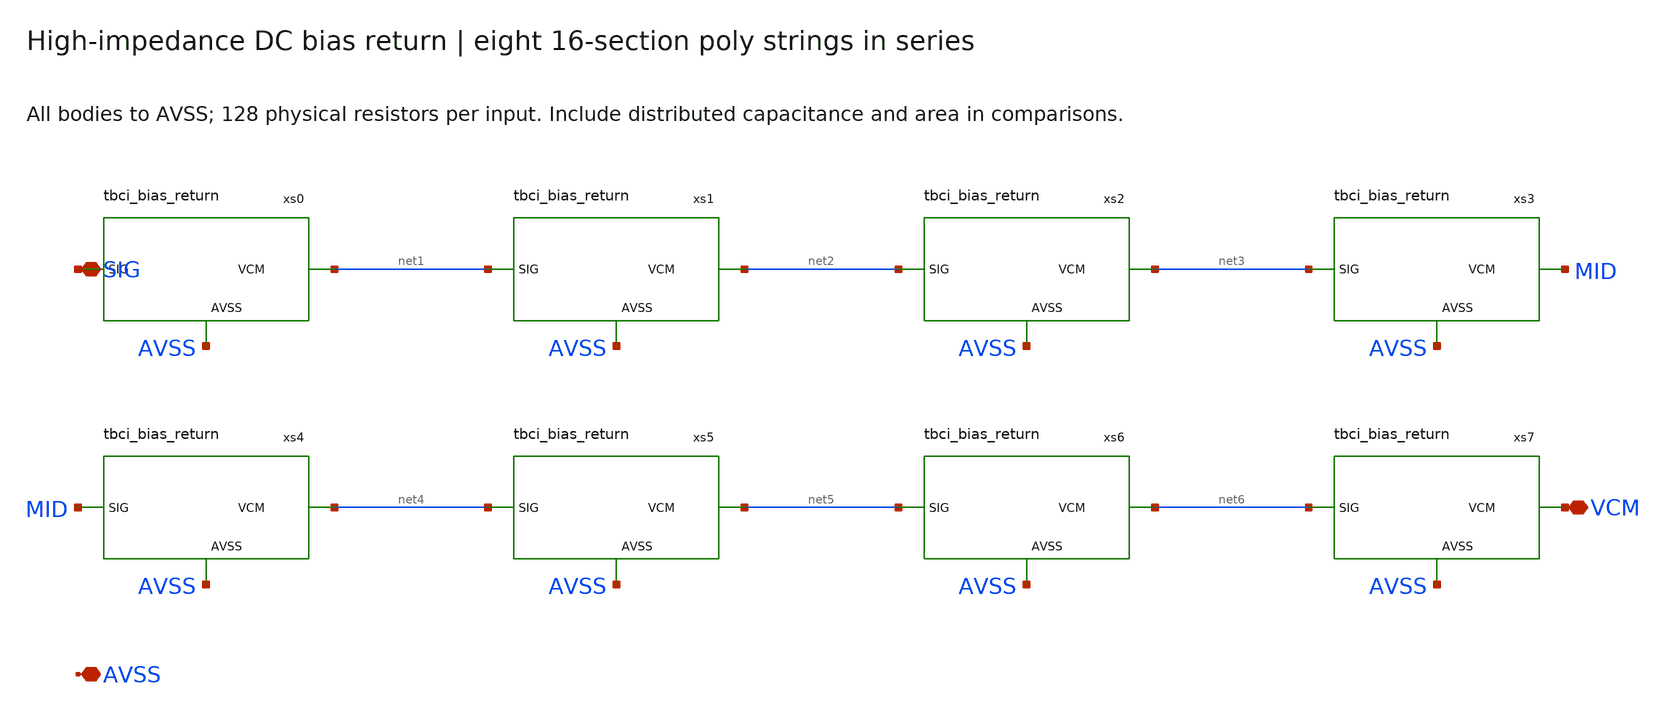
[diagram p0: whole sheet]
** sch_path: afe/xschem/tbci_bias_chain.sch
**.subckt tbci_bias_chain SIG VCM AVSS
*.iopin SIG
*.iopin VCM
*.iopin AVSS
xs0 SIG net1 AVSS tbci_bias_return
xs1 net1 net2 AVSS tbci_bias_return
xs2 net2 net3 AVSS tbci_bias_return
xs3 net3 MID AVSS tbci_bias_return
xs4 MID net4 AVSS tbci_bias_return
xs5 net4 net5 AVSS tbci_bias_return
xs6 net5 net6 AVSS tbci_bias_return
xs7 net6 VCM AVSS tbci_bias_return
**.ends

* expanding   symbol:  tbci_bias_return.sym # of pins=3
** sym_path: afe/xschem/tbci_bias_return.sym
** sch_path: afe/xschem/tbci_bias_return.sch
.subckt tbci_bias_return SIG VCM AVSS
*.iopin SIG
*.iopin VCM
*.iopin AVSS
XR0 net1 SIG AVSS sky130_fd_pr__res_xhigh_po_0p35 L=860 mult=1 m=1
XR1 net2 net1 AVSS sky130_fd_pr__res_xhigh_po_0p35 L=860 mult=1 m=1
XR2 net3 net2 AVSS sky130_fd_pr__res_xhigh_po_0p35 L=860 mult=1 m=1
XR3 net4 net3 AVSS sky130_fd_pr__res_xhigh_po_0p35 L=860 mult=1 m=1
XR4 net4 net5 AVSS sky130_fd_pr__res_xhigh_po_0p35 L=860 mult=1 m=1
XR5 net5 net6 AVSS sky130_fd_pr__res_xhigh_po_0p35 L=860 mult=1 m=1
XR6 net6 net7 AVSS sky130_fd_pr__res_xhigh_po_0p35 L=860 mult=1 m=1
XR7 net7 net8 AVSS sky130_fd_pr__res_xhigh_po_0p35 L=860 mult=1 m=1
XR8 net9 net8 AVSS sky130_fd_pr__res_xhigh_po_0p35 L=860 mult=1 m=1
XR9 net10 net9 AVSS sky130_fd_pr__res_xhigh_po_0p35 L=860 mult=1 m=1
XR10 net11 net10 AVSS sky130_fd_pr__res_xhigh_po_0p35 L=860 mult=1 m=1
XR11 net12 net11 AVSS sky130_fd_pr__res_xhigh_po_0p35 L=860 mult=1 m=1
XR12 net12 net13 AVSS sky130_fd_pr__res_xhigh_po_0p35 L=860 mult=1 m=1
XR13 net13 net14 AVSS sky130_fd_pr__res_xhigh_po_0p35 L=860 mult=1 m=1
XR14 net14 net15 AVSS sky130_fd_pr__res_xhigh_po_0p35 L=860 mult=1 m=1
XR15 net15 VCM AVSS sky130_fd_pr__res_xhigh_po_0p35 L=860 mult=1 m=1
.ends

.end
